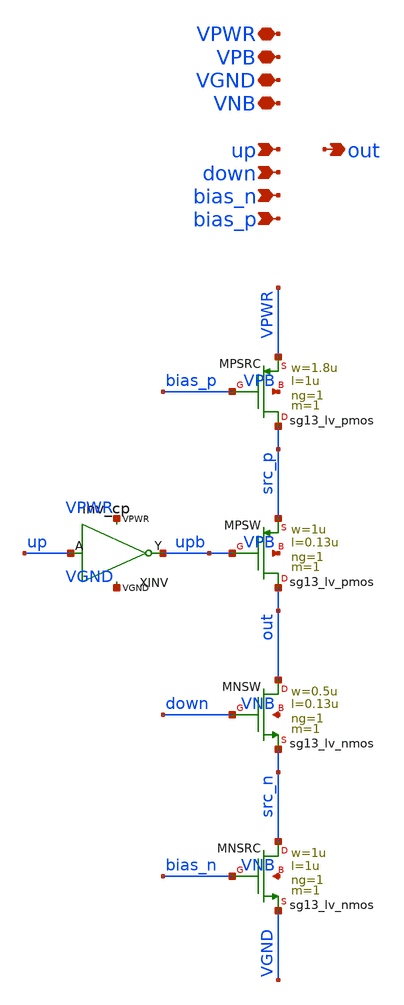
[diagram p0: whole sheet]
** sch_path: xschem/tiny_pll_charge_pump.sch
**.subckt tiny_pll_charge_pump up down VNB VGND VPB VPWR out bias_n bias_p
*.ipin up
*.ipin down
*.iopin VNB
*.iopin VGND
*.iopin VPB
*.iopin VPWR
*.opin out
*.ipin bias_n
*.ipin bias_p
XMNSRC src_n bias_n VGND VNB sg13_lv_nmos w=1u l=1u ng=1 m=1 mm_ok=1
XMNSW out down src_n VNB sg13_lv_nmos w=0.5u l=0.13u ng=1 m=1 mm_ok=1
XMPSW out upb src_p VPB sg13_lv_pmos w=1u l=0.13u ng=1 m=1 mm_ok=1
XMPSRC src_p bias_p VPWR VPB sg13_lv_pmos w=1.8u l=1u ng=1 m=1 mm_ok=1
XINV up upb VPWR VGND inv_cp
**.ends

* expanding   symbol:  inv_cp.sym # of pins=4
** sym_path: xschem/inv_cp.sym
** sch_path: xschem/inv_cp.sch
.subckt inv_cp A Y VPWR VGND
*.ipin A
*.opin Y
*.iopin VPWR
*.iopin VGND
XMP Y A VPWR VPWR sg13_lv_pmos w=2u l=0.13u ng=1 m=1 mm_ok=1
XMN Y A VGND VGND sg13_lv_nmos w=1u l=0.13u ng=1 m=1 mm_ok=1
.ends

.end
